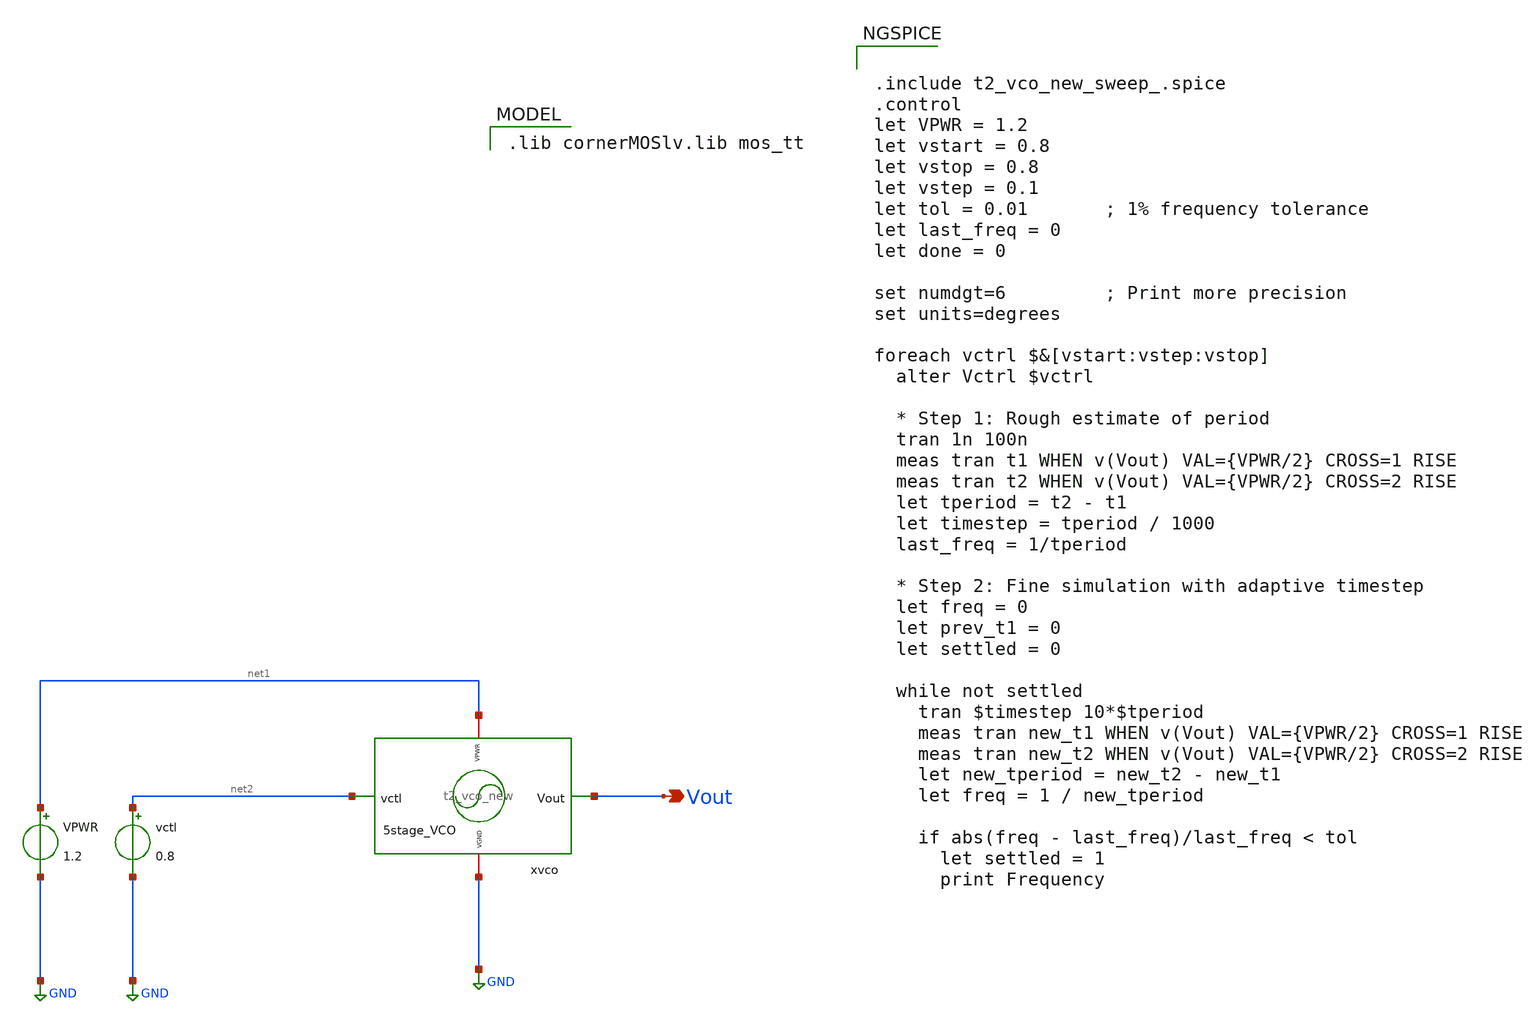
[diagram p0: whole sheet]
** sch_path: Team 2 Design/design_data/xschem/t2_vco_new_sweep_.sch
**.subckt t2_vco_new_sweep_ Vout
*.opin Vout
x1 net1 GND net2 Vout t2_vco_new
VPWR net1 GND 1.2
vctl net2 GND 0.8
**** begin user architecture code
 .lib cornerMOSlv.lib mos_tt



.include t2_vco_new_sweep_.spice
.control
let VPWR = 1.2
let vstart = 0.8
let vstop = 0.8
let vstep = 0.1
let tol = 0.01       ; 1% frequency tolerance
let last_freq = 0
let done = 0

set numdgt=6         ; Print more precision
set units=degrees

foreach vctrl $&[vstart:vstep:vstop]
  alter Vctrl $vctrl

  * Step 1: Rough estimate of period
  tran 1n 100n
  meas tran t1 WHEN v(Vout) VAL={VPWR/2} CROSS=1 RISE
  meas tran t2 WHEN v(Vout) VAL={VPWR/2} CROSS=2 RISE
  let tperiod = t2 - t1
  let timestep = tperiod / 1000
  last_freq = 1/tperiod

  * Step 2: Fine simulation with adaptive timestep
  let freq = 0
  let prev_t1 = 0
  let settled = 0

  while not settled
    tran $timestep 10*$tperiod
    meas tran new_t1 WHEN v(Vout) VAL={VPWR/2} CROSS=1 RISE
    meas tran new_t2 WHEN v(Vout) VAL={VPWR/2} CROSS=2 RISE
    let new_tperiod = new_t2 - new_t1
    let freq = 1 / new_tperiod

    if abs(freq - last_freq)/last_freq < tol
      let settled = 1
      print Frequency

**** end user architecture code
**.ends
.GLOBAL GND
.end
